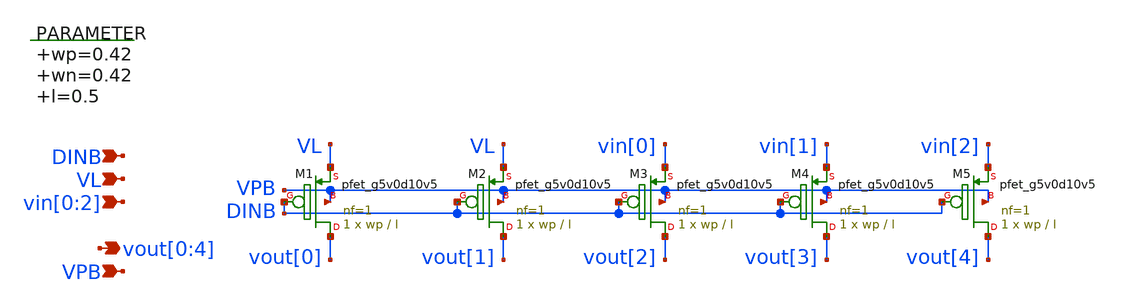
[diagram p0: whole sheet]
** sch_path: xschem/seg_selector_3.sch
**.subckt seg_selector_3 vout[0],vout[1],vout[2],vout[3],vout[4] VPB DINB vin[0],vin[1],vin[2] VL
*.opin vout[0],vout[1],vout[2],vout[3],vout[4]
*.ipin VPB
*.ipin DINB
*.ipin vin[0],vin[1],vin[2]
*.ipin VL
.param wp=0.42 wn=0.42 l=0.5

XM1 vout[0] DINB VL VPB sky130_fd_pr__pfet_g5v0d10v5 L=l W=wp nf=1 ad='int((nf+1)/2) * W/nf * 0.29' as='int((nf+2)/2) * W/nf * 0.29'
+ pd='2*int((nf+1)/2) * (W/nf + 0.29)' ps='2*int((nf+2)/2) * (W/nf + 0.29)' nrd='0.29 / W' nrs='0.29 / W'
+ sa=0 sb=0 sd=0 mult=1 m=1
XM2 vout[1] DINB VL VPB sky130_fd_pr__pfet_g5v0d10v5 L=l W=wp nf=1 ad='int((nf+1)/2) * W/nf * 0.29' as='int((nf+2)/2) * W/nf * 0.29'
+ pd='2*int((nf+1)/2) * (W/nf + 0.29)' ps='2*int((nf+2)/2) * (W/nf + 0.29)' nrd='0.29 / W' nrs='0.29 / W'
+ sa=0 sb=0 sd=0 mult=1 m=1
XM3 vout[2] DINB vin[0] VPB sky130_fd_pr__pfet_g5v0d10v5 L=l W=wp nf=1 ad='int((nf+1)/2) * W/nf * 0.29'
+ as='int((nf+2)/2) * W/nf * 0.29' pd='2*int((nf+1)/2) * (W/nf + 0.29)' ps='2*int((nf+2)/2) * (W/nf + 0.29)'
+ nrd='0.29 / W' nrs='0.29 / W' sa=0 sb=0 sd=0 mult=1 m=1
XM4 vout[3] DINB vin[1] VPB sky130_fd_pr__pfet_g5v0d10v5 L=l W=wp nf=1 ad='int((nf+1)/2) * W/nf * 0.29'
+ as='int((nf+2)/2) * W/nf * 0.29' pd='2*int((nf+1)/2) * (W/nf + 0.29)' ps='2*int((nf+2)/2) * (W/nf + 0.29)'
+ nrd='0.29 / W' nrs='0.29 / W' sa=0 sb=0 sd=0 mult=1 m=1
XM5 vout[4] DINB vin[2] VPB sky130_fd_pr__pfet_g5v0d10v5 L=l W=wp nf=1 ad='int((nf+1)/2) * W/nf * 0.29'
+ as='int((nf+2)/2) * W/nf * 0.29' pd='2*int((nf+1)/2) * (W/nf + 0.29)' ps='2*int((nf+2)/2) * (W/nf + 0.29)'
+ nrd='0.29 / W' nrs='0.29 / W' sa=0 sb=0 sd=0 mult=1 m=1
**.ends
.end
